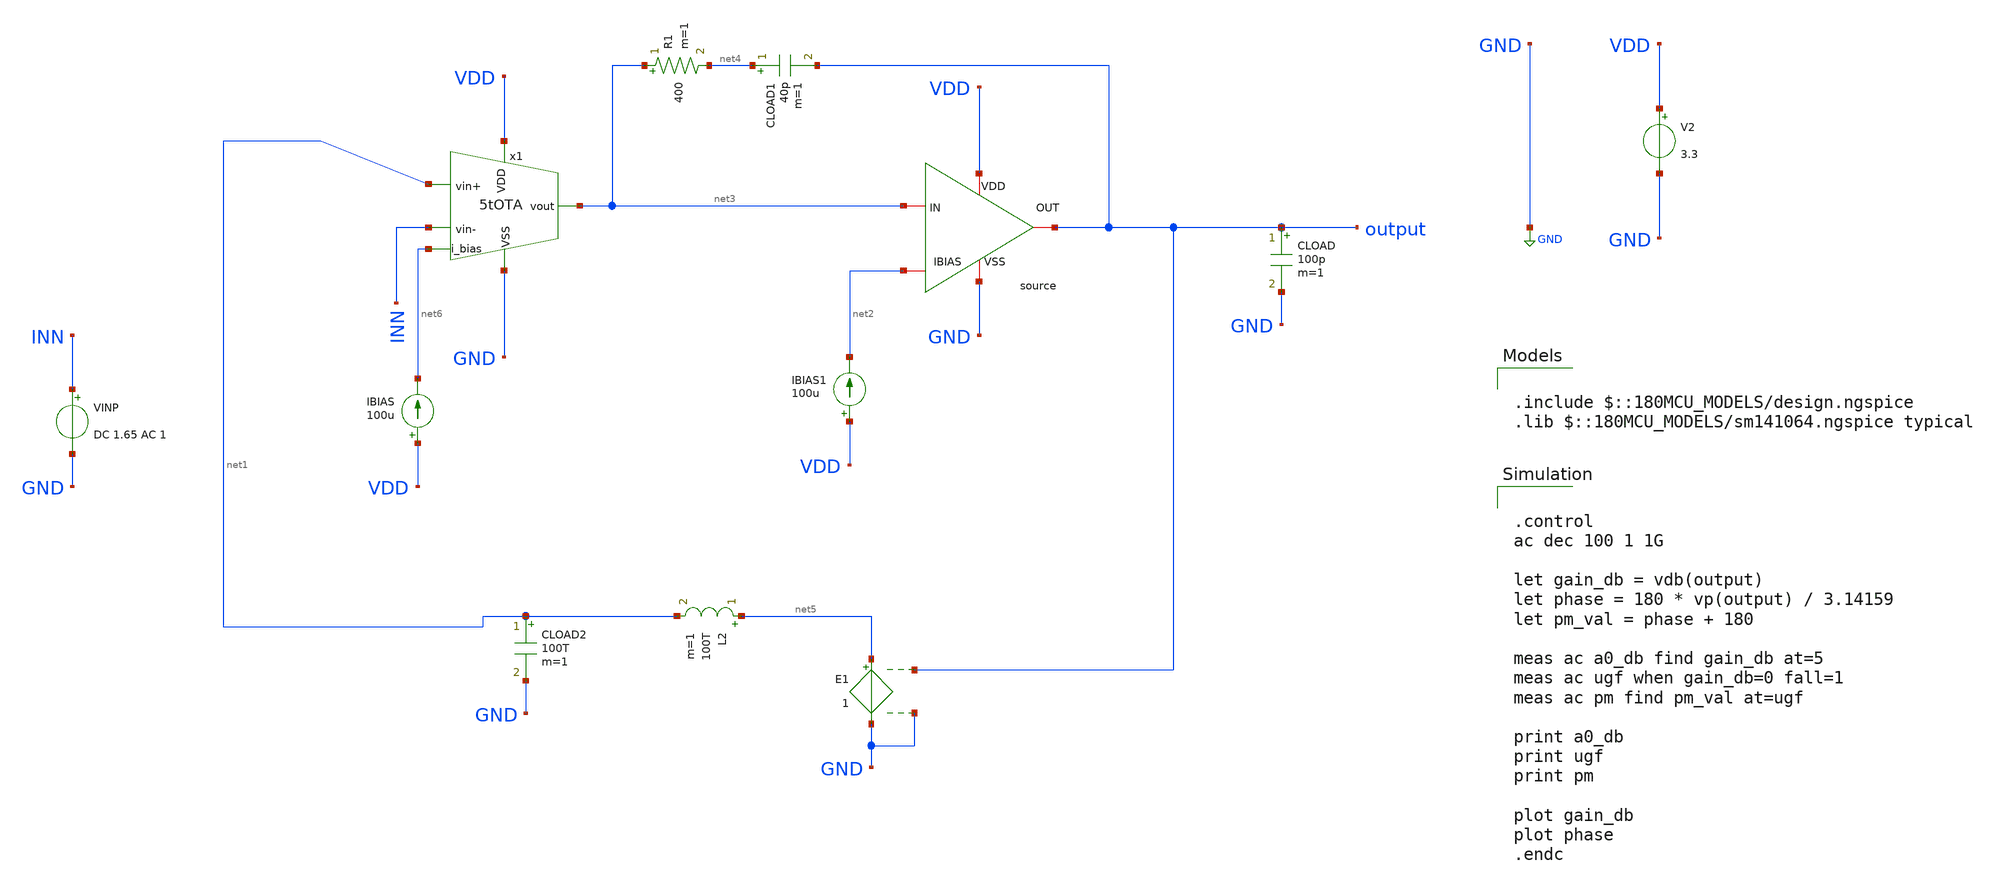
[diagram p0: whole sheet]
** sch_path: designs/libs/core_amps/two_stage_amps/5t_cs_ac_tb.sch
**.subckt 5t_cs_ac_tb
x2 VDD net3 net2 output GND cs_schematic
V2 VDD GND 3.3
IBIAS VDD net6 100u
IBIAS1 VDD net2 100u
CLOAD output GND 100p m=1
CLOAD1 net4 output 40p m=1
R1 net3 net4 400 m=1
VINP INN GND DC 1.65 AC 1
L2 net5 net1 100T m=1
CLOAD2 net1 GND 100T m=1
E1 net5 GND output GND 1
x1 VDD net3 net1 INN net6 net7 5tOTA
**** begin user architecture code

.include $::180MCU_MODELS/design.ngspice
.lib $::180MCU_MODELS/sm141064.ngspice typical



.control
ac dec 100 1 1G

let gain_db = vdb(output)
let phase = 180 * vp(output) / 3.14159
let pm_val = phase + 180

meas ac a0_db find gain_db at=5
meas ac ugf when gain_db=0 fall=1
meas ac pm find pm_val at=ugf

print a0_db
print ugf
print pm

plot gain_db
plot phase
.endc


**** end user architecture code
**.ends
.GLOBAL GND
.end
